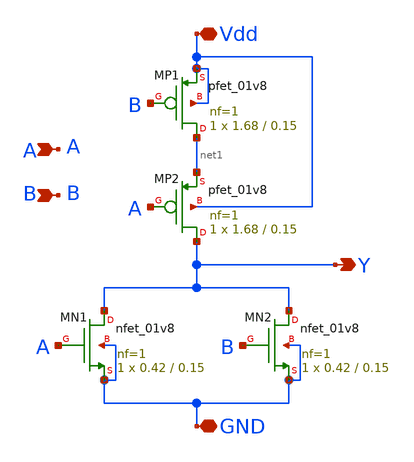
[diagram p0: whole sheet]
** sch_path: xschem_project/nor2/nor2_lvsclean.sch
**.subckt nor2_lvsclean Vdd A B Y GND
*.iopin Vdd
*.ipin A
*.ipin B
*.opin Y
*.iopin GND
XMP1 net1 B Vdd Vdd sky130_fd_pr__pfet_01v8 L=0.15 W=1.68 nf=1 ad='int((1 + 1)/2) * 1.68 / 1 * 0.29'
+ as='int((1 + 2)/2) * 1.68 / 1 * 0.29' pd='2*int((1 + 1)/2) * (1.68 / 1 + 0.29)' ps='2*int((1 + 2)/2) * (1.68 / 1 + 0.29)'
+ nrd='0.29 / 1.68 ' nrs='0.29 / 1.68 ' sa=0 sb=0 sd=0 mult=1 m=1
XMP2 Y A net1 Vdd sky130_fd_pr__pfet_01v8 L=0.15 W=1.68 nf=1 ad='int((1 + 1)/2) * 1.68 / 1 * 0.29' as='int((1 + 2)/2) * 1.68 / 1 * 0.29'
+ pd='2*int((1 + 1)/2) * (1.68 / 1 + 0.29)' ps='2*int((1 + 2)/2) * (1.68 / 1 + 0.29)' nrd='0.29 / 1.68 '
+ nrs='0.29 / 1.68 ' sa=0 sb=0 sd=0 mult=1 m=1
XMN1 Y A GND GND sky130_fd_pr__nfet_01v8 L=0.15 W=0.42 nf=1 ad='int((1 + 1)/2) * 0.42 / 1 * 0.29' as='int((1 + 2)/2) * 0.42 / 1 * 0.29'
+ pd='2*int((1 + 1)/2) * (0.42 / 1 + 0.29)' ps='2*int((1 + 2)/2) * (0.42 / 1 + 0.29)' nrd='0.29 / 0.42 '
+ nrs='0.29 / 0.42 ' sa=0 sb=0 sd=0 mult=1 m=1
XMN2 Y B GND GND sky130_fd_pr__nfet_01v8 L=0.15 W=0.42 nf=1 ad='int((1 + 1)/2) * 0.42 / 1 * 0.29' as='int((1 + 2)/2) * 0.42 / 1 * 0.29'
+ pd='2*int((1 + 1)/2) * (0.42 / 1 + 0.29)' ps='2*int((1 + 2)/2) * (0.42 / 1 + 0.29)' nrd='0.29 / 0.42 '
+ nrs='0.29 / 0.42 ' sa=0 sb=0 sd=0 mult=1 m=1
**.ends
.end
